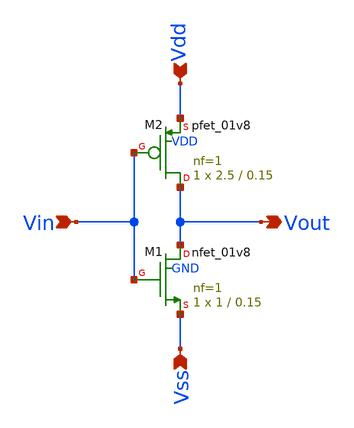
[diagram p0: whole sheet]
** sch_path: Xschem/inv.sch
**.subckt inv Vin Vss Vdd Vout
*.ipin Vin
*.ipin Vss
*.ipin Vdd
*.opin Vout
XM1 Vout Vin Vss GND sky130_fd_pr__nfet_01v8 L=0.15 W=1 nf=1 ad='int((nf+1)/2) * W/nf * 0.29' as='int((nf+2)/2) * W/nf * 0.29'
+ pd='2*int((nf+1)/2) * (W/nf + 0.29)' ps='2*int((nf+2)/2) * (W/nf + 0.29)' nrd='0.29 / W' nrs='0.29 / W'
+ sa=0 sb=0 sd=0 mult=1 m=1
XM2 Vout Vin Vdd VDD sky130_fd_pr__pfet_01v8 L=0.15 W=2.5 nf=1 ad='int((nf+1)/2) * W/nf * 0.29' as='int((nf+2)/2) * W/nf * 0.29'
+ pd='2*int((nf+1)/2) * (W/nf + 0.29)' ps='2*int((nf+2)/2) * (W/nf + 0.29)' nrd='0.29 / W' nrs='0.29 / W'
+ sa=0 sb=0 sd=0 mult=1 m=1
**.ends
.end
